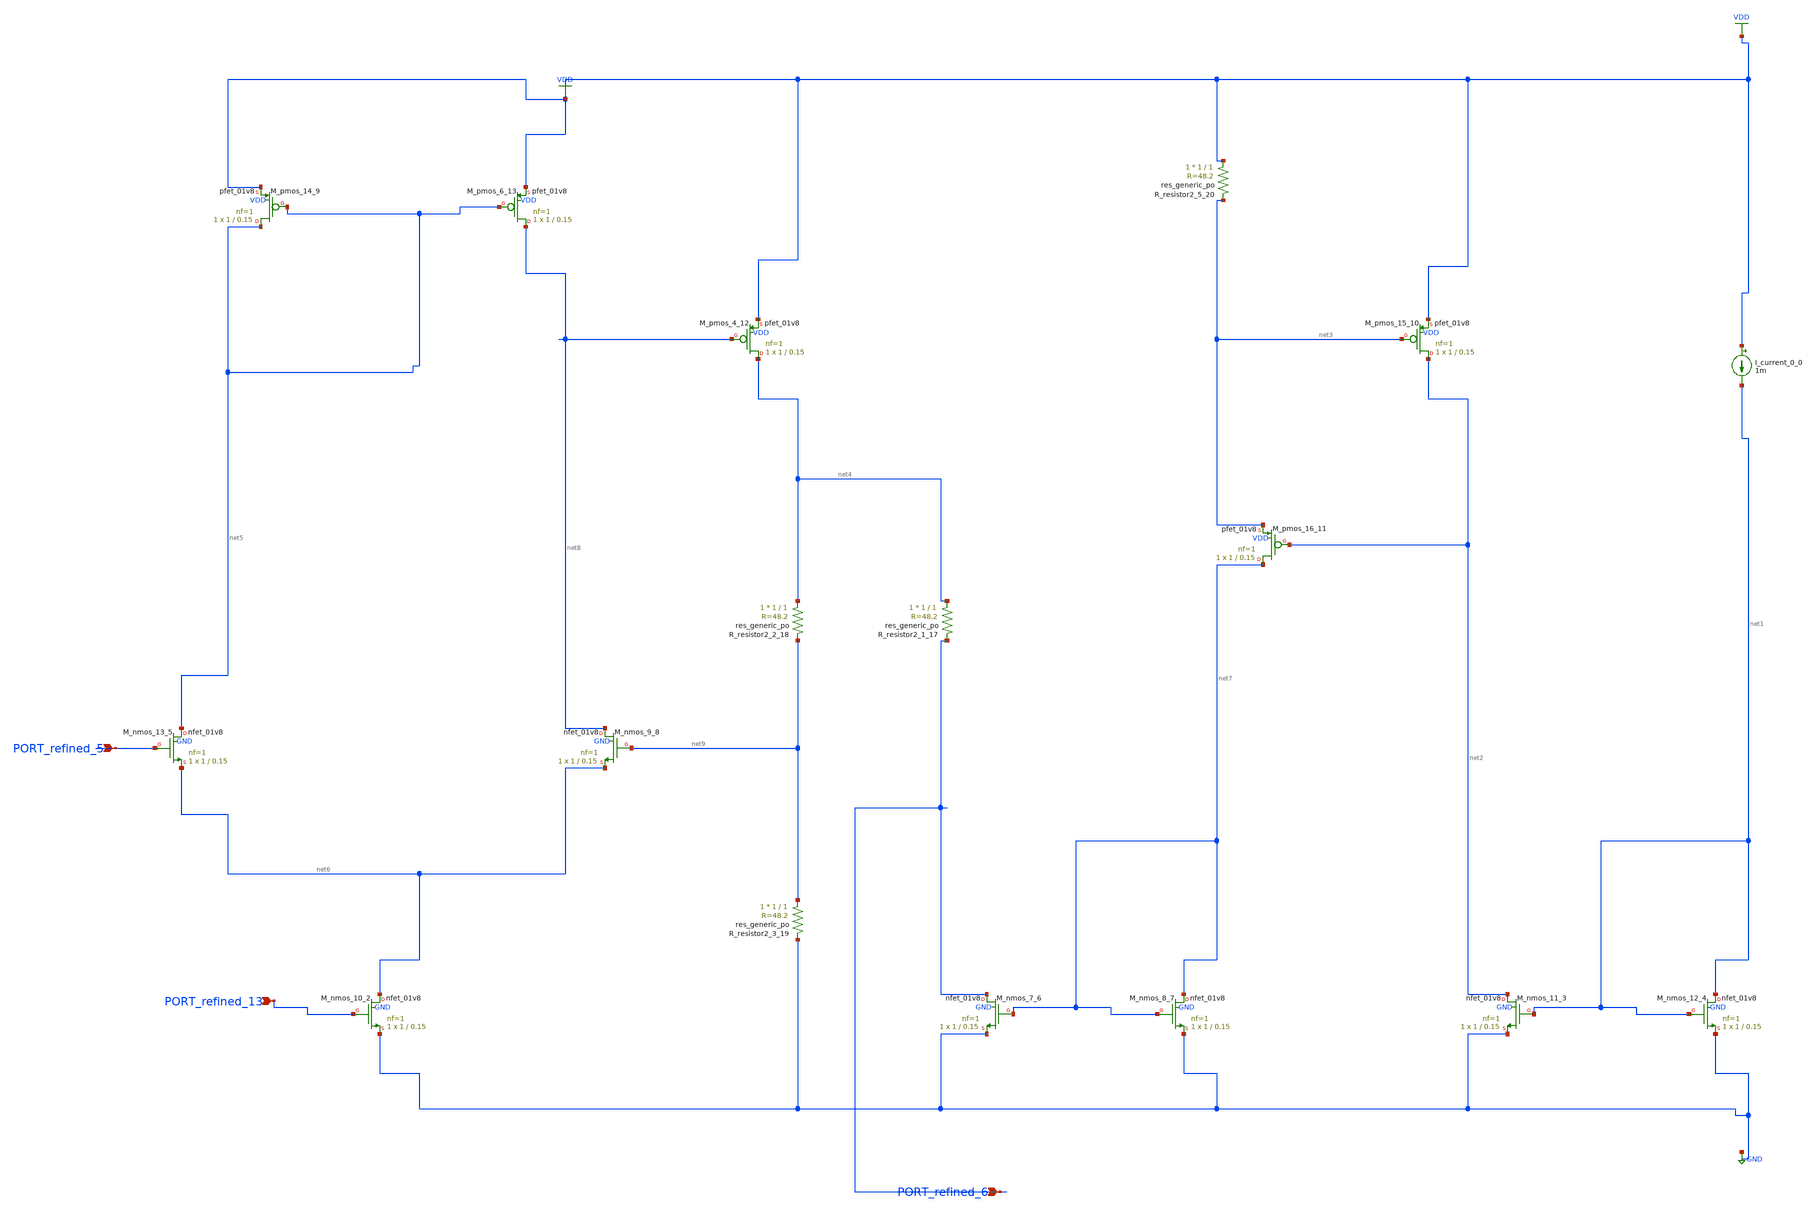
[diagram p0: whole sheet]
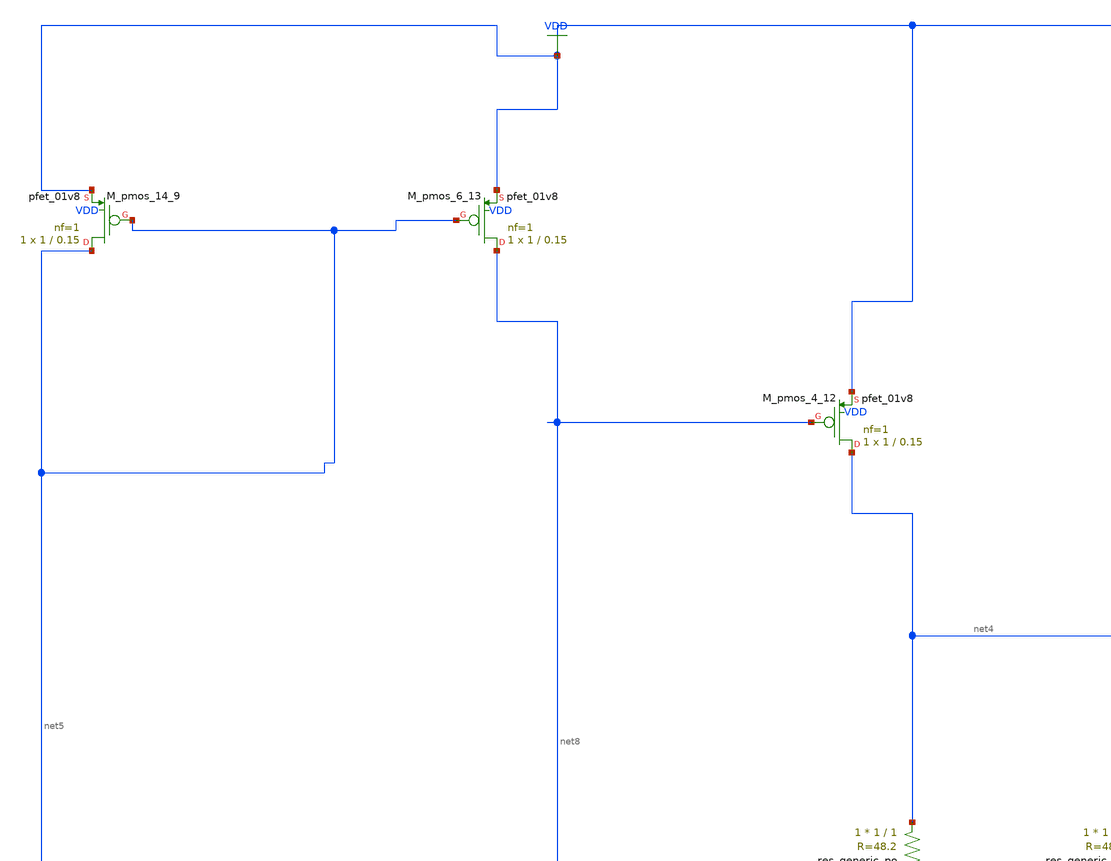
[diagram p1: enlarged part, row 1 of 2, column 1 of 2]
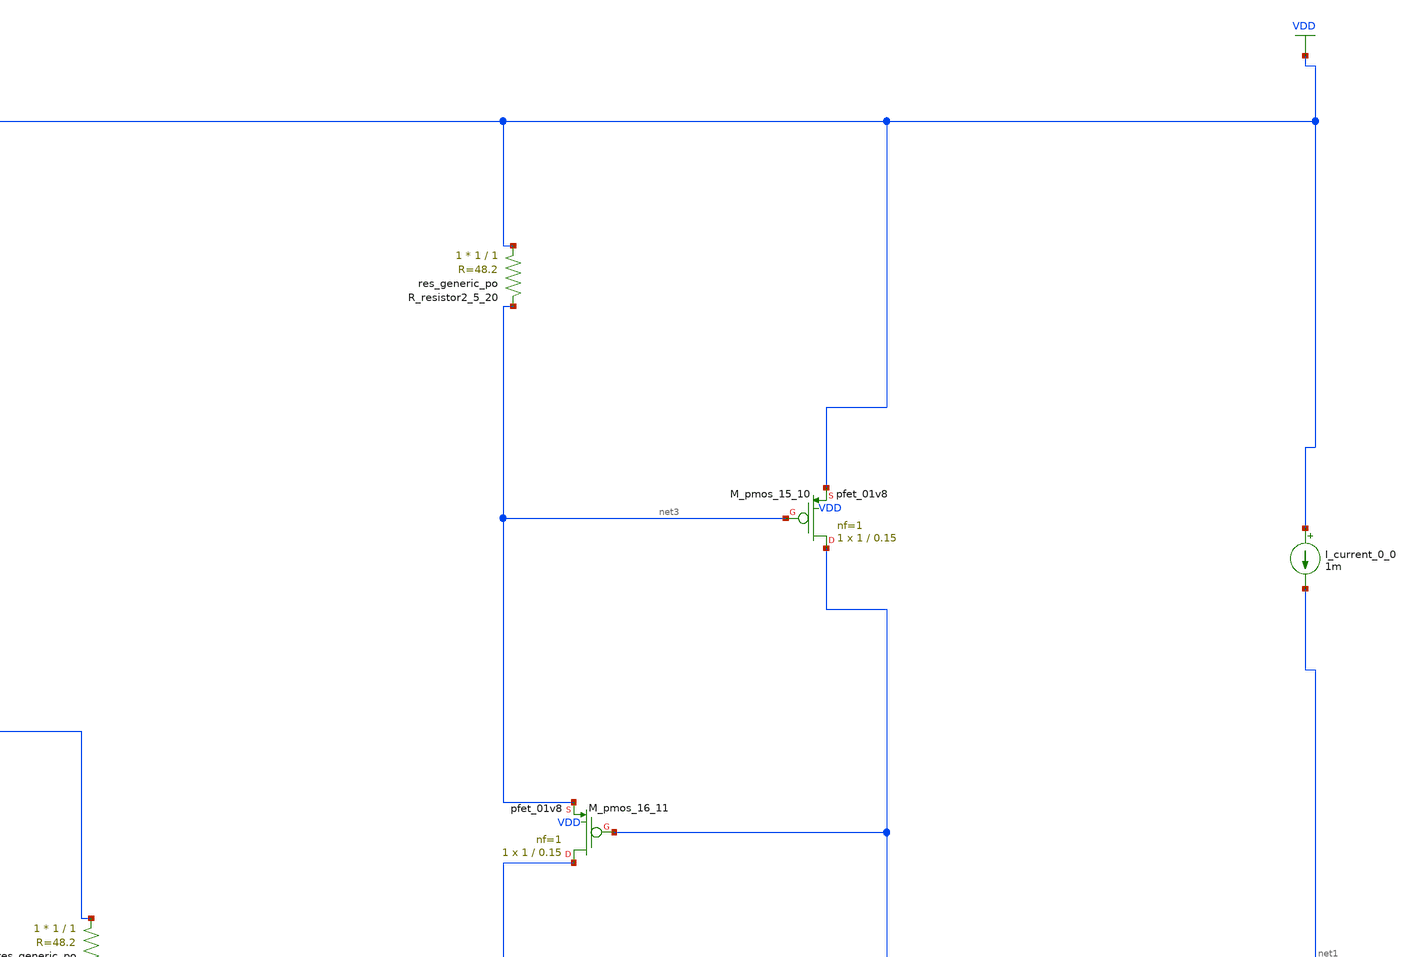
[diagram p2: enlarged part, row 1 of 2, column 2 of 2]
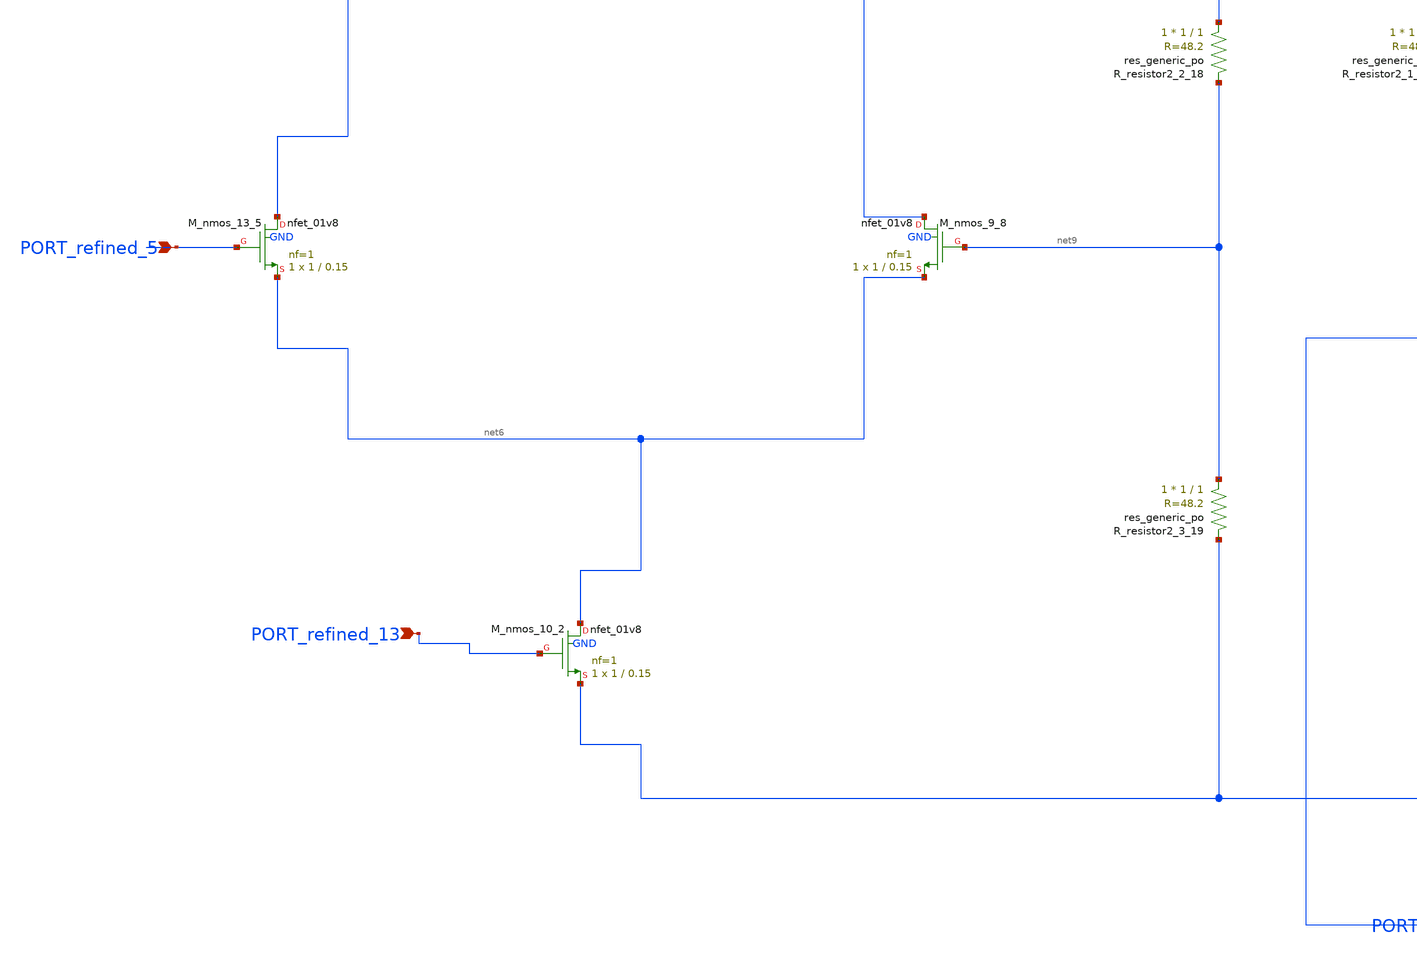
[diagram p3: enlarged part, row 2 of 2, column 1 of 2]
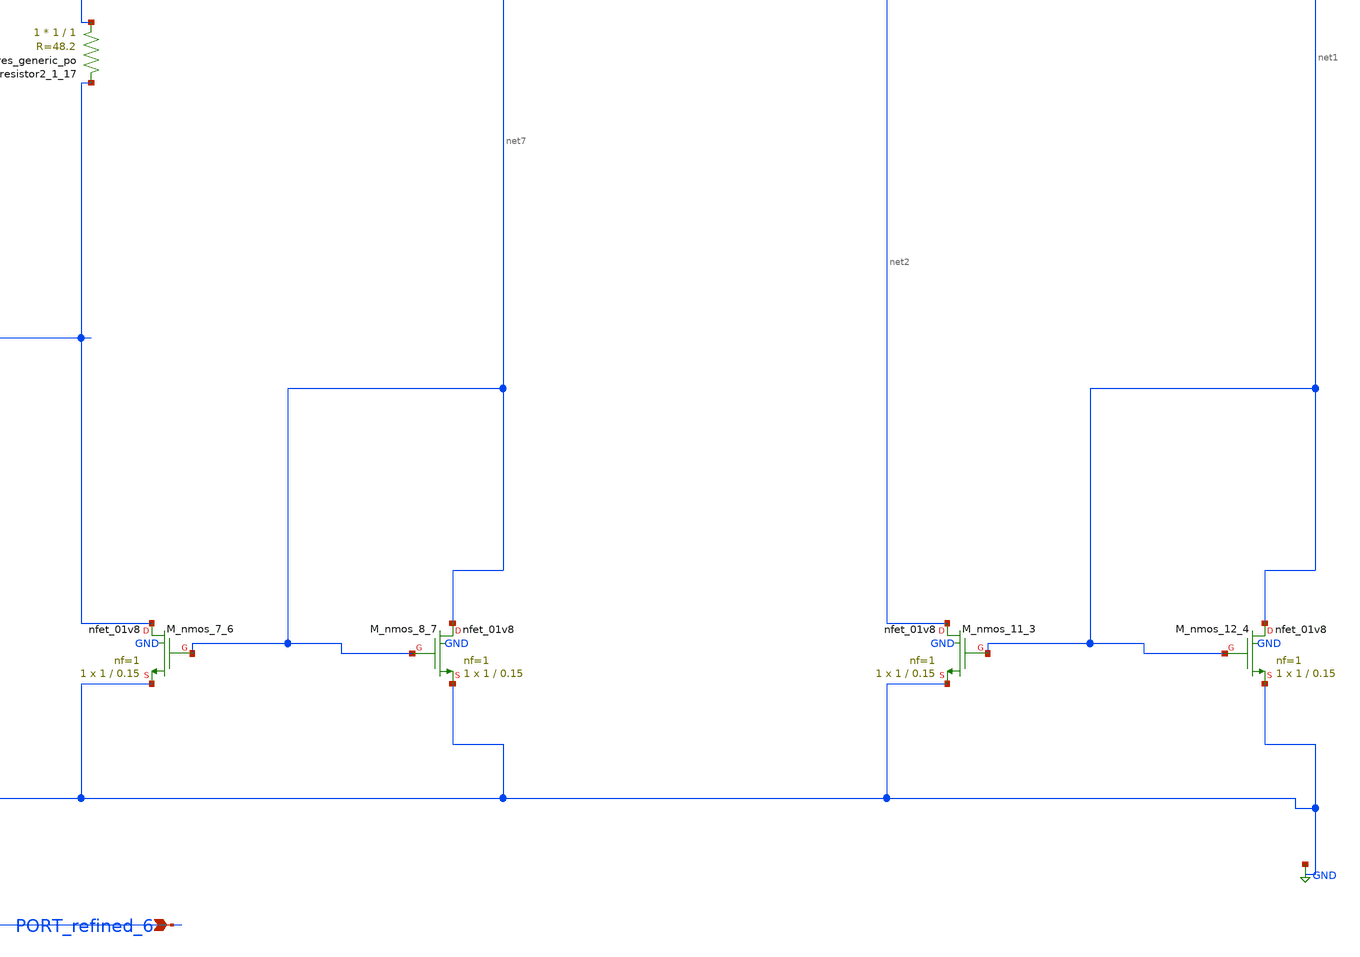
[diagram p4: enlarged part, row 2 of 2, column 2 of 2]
** sch_path: schematics/SchemGen/10_1109_PRIME_2014_6872677_08_002.sch
**.subckt 10_1109_PRIME_2014_6872677_08_002 PORT_refined_6 PORT_refined_13 PORT_refined_5
*.ipin PORT_refined_6
*.ipin PORT_refined_13
*.ipin PORT_refined_5
I_current_0_0 VDD net1 1m
XM_nmos_10_2 net6 PORT_refined_13 GND GND sky130_fd_pr__nfet_01v8 L=0.15 W=1 nf=1 ad='int((1 + 1)/2) * 1 / 1 * 0.29'
+ as='int((1 + 2)/2) * 1 / 1 * 0.29' pd='2*int((1 + 1)/2) * (1 / 1 + 0.29)' ps='2*int((1 + 2)/2) * (1 / 1 + 0.29)'
+ nrd='0.29 / 1 ' nrs='0.29 / 1 ' sa=0 sb=0 sd=0 mult=1 m=1
XM_nmos_11_3 net2 net1 GND GND sky130_fd_pr__nfet_01v8 L=0.15 W=1 nf=1 ad='int((1 + 1)/2) * 1 / 1 * 0.29'
+ as='int((1 + 2)/2) * 1 / 1 * 0.29' pd='2*int((1 + 1)/2) * (1 / 1 + 0.29)' ps='2*int((1 + 2)/2) * (1 / 1 + 0.29)'
+ nrd='0.29 / 1 ' nrs='0.29 / 1 ' sa=0 sb=0 sd=0 mult=1 m=1
XM_nmos_12_4 net1 net1 GND GND sky130_fd_pr__nfet_01v8 L=0.15 W=1 nf=1 ad='int((1 + 1)/2) * 1 / 1 * 0.29'
+ as='int((1 + 2)/2) * 1 / 1 * 0.29' pd='2*int((1 + 1)/2) * (1 / 1 + 0.29)' ps='2*int((1 + 2)/2) * (1 / 1 + 0.29)'
+ nrd='0.29 / 1 ' nrs='0.29 / 1 ' sa=0 sb=0 sd=0 mult=1 m=1
XM_nmos_13_5 net5 PORT_refined_5 net6 GND sky130_fd_pr__nfet_01v8 L=0.15 W=1 nf=1 ad='int((1 + 1)/2) * 1 / 1 * 0.29'
+ as='int((1 + 2)/2) * 1 / 1 * 0.29' pd='2*int((1 + 1)/2) * (1 / 1 + 0.29)' ps='2*int((1 + 2)/2) * (1 / 1 + 0.29)'
+ nrd='0.29 / 1 ' nrs='0.29 / 1 ' sa=0 sb=0 sd=0 mult=1 m=1
XM_nmos_7_6 PORT_refined_6 net7 GND GND sky130_fd_pr__nfet_01v8 L=0.15 W=1 nf=1 ad='int((1 + 1)/2) * 1 / 1 * 0.29'
+ as='int((1 + 2)/2) * 1 / 1 * 0.29' pd='2*int((1 + 1)/2) * (1 / 1 + 0.29)' ps='2*int((1 + 2)/2) * (1 / 1 + 0.29)'
+ nrd='0.29 / 1 ' nrs='0.29 / 1 ' sa=0 sb=0 sd=0 mult=1 m=1
XM_nmos_8_7 net7 net7 GND GND sky130_fd_pr__nfet_01v8 L=0.15 W=1 nf=1 ad='int((1 + 1)/2) * 1 / 1 * 0.29'
+ as='int((1 + 2)/2) * 1 / 1 * 0.29' pd='2*int((1 + 1)/2) * (1 / 1 + 0.29)' ps='2*int((1 + 2)/2) * (1 / 1 + 0.29)'
+ nrd='0.29 / 1 ' nrs='0.29 / 1 ' sa=0 sb=0 sd=0 mult=1 m=1
XM_nmos_9_8 net8 net9 net6 GND sky130_fd_pr__nfet_01v8 L=0.15 W=1 nf=1 ad='int((1 + 1)/2) * 1 / 1 * 0.29'
+ as='int((1 + 2)/2) * 1 / 1 * 0.29' pd='2*int((1 + 1)/2) * (1 / 1 + 0.29)' ps='2*int((1 + 2)/2) * (1 / 1 + 0.29)'
+ nrd='0.29 / 1 ' nrs='0.29 / 1 ' sa=0 sb=0 sd=0 mult=1 m=1
XM_pmos_14_9 net5 net5 VDD VDD sky130_fd_pr__pfet_01v8 L=0.15 W=1 nf=1 ad='int((1 + 1)/2) * 1 / 1 * 0.29'
+ as='int((1 + 2)/2) * 1 / 1 * 0.29' pd='2*int((1 + 1)/2) * (1 / 1 + 0.29)' ps='2*int((1 + 2)/2) * (1 / 1 + 0.29)'
+ nrd='0.29 / 1 ' nrs='0.29 / 1 ' sa=0 sb=0 sd=0 mult=1 m=1
XM_pmos_15_10 net2 net3 VDD VDD sky130_fd_pr__pfet_01v8 L=0.15 W=1 nf=1 ad='int((1 + 1)/2) * 1 / 1 * 0.29'
+ as='int((1 + 2)/2) * 1 / 1 * 0.29' pd='2*int((1 + 1)/2) * (1 / 1 + 0.29)' ps='2*int((1 + 2)/2) * (1 / 1 + 0.29)'
+ nrd='0.29 / 1 ' nrs='0.29 / 1 ' sa=0 sb=0 sd=0 mult=1 m=1
XM_pmos_16_11 net7 net2 net3 VDD sky130_fd_pr__pfet_01v8 L=0.15 W=1 nf=1 ad='int((1 + 1)/2) * 1 / 1 * 0.29'
+ as='int((1 + 2)/2) * 1 / 1 * 0.29' pd='2*int((1 + 1)/2) * (1 / 1 + 0.29)' ps='2*int((1 + 2)/2) * (1 / 1 + 0.29)'
+ nrd='0.29 / 1 ' nrs='0.29 / 1 ' sa=0 sb=0 sd=0 mult=1 m=1
XM_pmos_4_12 net4 net8 VDD VDD sky130_fd_pr__pfet_01v8 L=0.15 W=1 nf=1 ad='int((1 + 1)/2) * 1 / 1 * 0.29'
+ as='int((1 + 2)/2) * 1 / 1 * 0.29' pd='2*int((1 + 1)/2) * (1 / 1 + 0.29)' ps='2*int((1 + 2)/2) * (1 / 1 + 0.29)'
+ nrd='0.29 / 1 ' nrs='0.29 / 1 ' sa=0 sb=0 sd=0 mult=1 m=1
XM_pmos_6_13 net8 net5 VDD VDD sky130_fd_pr__pfet_01v8 L=0.15 W=1 nf=1 ad='int((1 + 1)/2) * 1 / 1 * 0.29'
+ as='int((1 + 2)/2) * 1 / 1 * 0.29' pd='2*int((1 + 1)/2) * (1 / 1 + 0.29)' ps='2*int((1 + 2)/2) * (1 / 1 + 0.29)'
+ nrd='0.29 / 1 ' nrs='0.29 / 1 ' sa=0 sb=0 sd=0 mult=1 m=1
XR_resistor2_1_17 net4 PORT_refined_6 sky130_fd_pr__res_generic_po W=1 L=1 m=1
XR_resistor2_2_18 net4 net9 sky130_fd_pr__res_generic_po W=1 L=1 m=1
XR_resistor2_3_19 net9 GND sky130_fd_pr__res_generic_po W=1 L=1 m=1
XR_resistor2_5_20 VDD net3 sky130_fd_pr__res_generic_po W=1 L=1 m=1
**.ends
.GLOBAL GND
.GLOBAL VDD
.end
